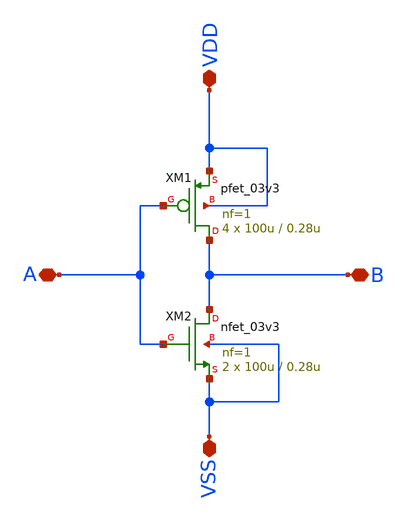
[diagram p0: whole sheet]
** sch_path: designs/ring_oscillator_pg/inverter/inv.sch
**.subckt inv VSS B A VDD
*.iopin VSS
*.iopin B
*.iopin A
*.iopin VDD
XM1 B A VDD VDD pfet_03v3 L=0.28u W=100u nf=1 ad='int((nf+1)/2) * W/nf * 0.18u' as='int((nf+2)/2) * W/nf * 0.18u'
+ pd='2*int((nf+1)/2) * (W/nf + 0.18u)' ps='2*int((nf+2)/2) * (W/nf + 0.18u)' nrd='0.18u / W' nrs='0.18u / W'
+ sa=0 sb=0 sd=0 m=4
XM2 B A VSS VSS nfet_03v3 L=0.28u W=100u nf=1 ad='int((nf+1)/2) * W/nf * 0.18u' as='int((nf+2)/2) * W/nf * 0.18u'
+ pd='2*int((nf+1)/2) * (W/nf + 0.18u)' ps='2*int((nf+2)/2) * (W/nf + 0.18u)' nrd='0.18u / W' nrs='0.18u / W'
+ sa=0 sb=0 sd=0 m=2
**.ends
.end
